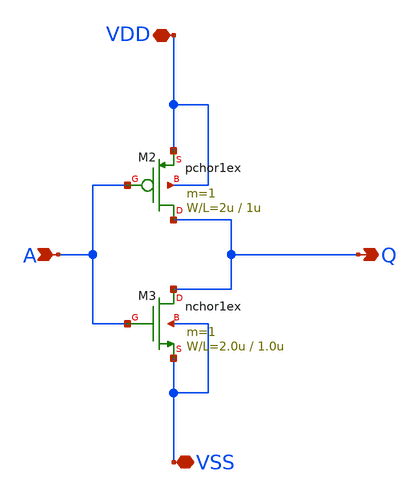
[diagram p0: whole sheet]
** sch_path: member_project/monmonmon/simon.sch
**.subckt simon Q A VSS VDD
*.opin Q
*.ipin A
*.iopin VSS
*.iopin VDD
M2 Q A VDD VDD pchor1ex L=1u W=2u m=1
M3 Q A VSS VSS nchor1ex L=1.0u W=2.0u m=1
**.ends
.end
